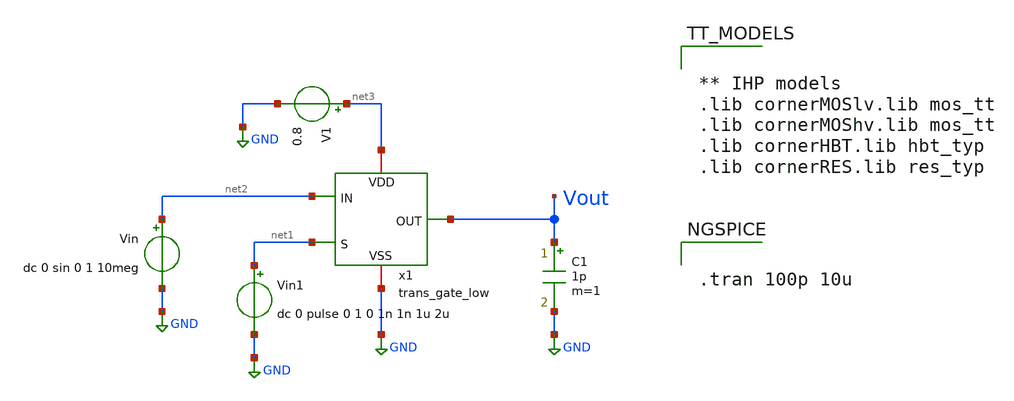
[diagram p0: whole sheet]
** sch_path: SSDOR_1.2V_v2/components/trans_gate_low/tb_tg_low.sch
**.subckt tb_tg_low
Vin net2 GND dc 0 sin 0 1 10meg
Vin1 net1 GND dc 0 pulse 0 1 0 1n 1n 1u 2u
V1 net3 GND 0.8
C1 Vout GND 1p m=1
x1 Vout net2 net3 net1 GND trans_gate_low
**** begin user architecture code


** IHP models
.lib cornerMOSlv.lib mos_tt
.lib cornerMOShv.lib mos_tt
.lib cornerHBT.lib hbt_typ
.lib cornerRES.lib res_typ




.tran 100p 10u


**** end user architecture code
**.ends
.GLOBAL GND
.end
